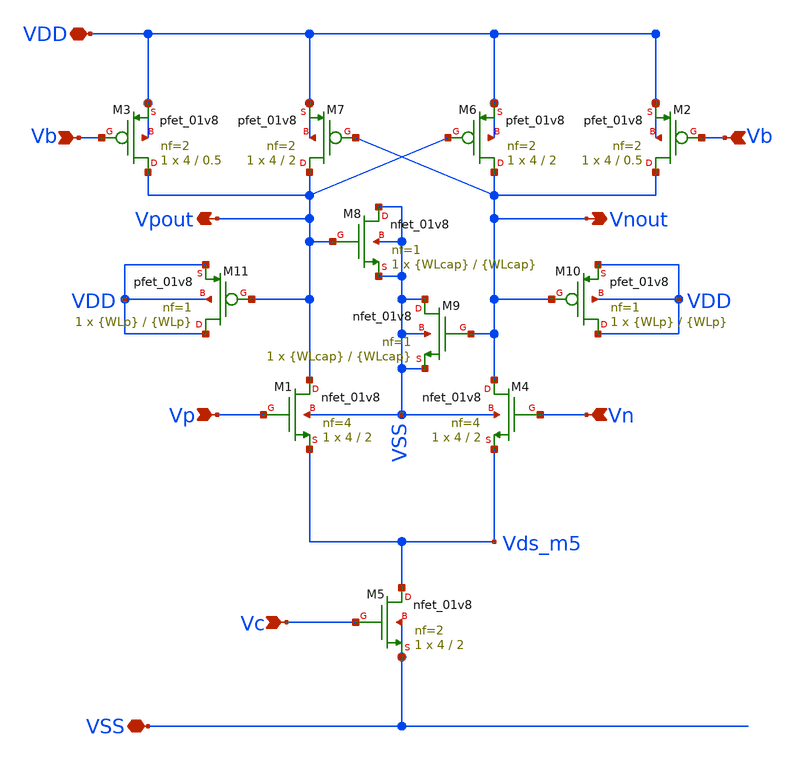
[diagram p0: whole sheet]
** sch_path: xschem/vco_stage_5.sch
**.subckt vco_stage_5 VDD VSS Vp Vn Vb Vc Vpout Vnout Vb
*.iopin VDD
*.iopin VSS
*.ipin Vp
*.ipin Vn
*.ipin Vb
*.ipin Vc
*.opin Vpout
*.opin Vnout
*.ipin Vb
XM1 Vpout Vp Vds_m5 VSS sky130_fd_pr__nfet_01v8 L=2 W=4 nf=4 ad='int((nf+1)/2) * W/nf * 0.29' as='int((nf+2)/2) * W/nf * 0.29'
+ pd='2*int((nf+1)/2) * (W/nf + 0.29)' ps='2*int((nf+2)/2) * (W/nf + 0.29)' nrd='0.29 / W' nrs='0.29 / W'
+ sa=0 sb=0 sd=0 mult=1 m=1
XM4 Vnout Vn Vds_m5 VSS sky130_fd_pr__nfet_01v8 L=2 W=4 nf=4 ad='int((nf+1)/2) * W/nf * 0.29' as='int((nf+2)/2) * W/nf * 0.29'
+ pd='2*int((nf+1)/2) * (W/nf + 0.29)' ps='2*int((nf+2)/2) * (W/nf + 0.29)' nrd='0.29 / W' nrs='0.29 / W'
+ sa=0 sb=0 sd=0 mult=1 m=1
XM5 Vds_m5 Vc VSS VSS sky130_fd_pr__nfet_01v8 L=2 W=4 nf=2 ad='int((nf+1)/2) * W/nf * 0.29' as='int((nf+2)/2) * W/nf * 0.29'
+ pd='2*int((nf+1)/2) * (W/nf + 0.29)' ps='2*int((nf+2)/2) * (W/nf + 0.29)' nrd='0.29 / W' nrs='0.29 / W'
+ sa=0 sb=0 sd=0 mult=1 m=1
XM2 Vnout Vb VDD VDD sky130_fd_pr__pfet_01v8 L=0.5 W=4 nf=2 ad='int((nf+1)/2) * W/nf * 0.29' as='int((nf+2)/2) * W/nf * 0.29'
+ pd='2*int((nf+1)/2) * (W/nf + 0.29)' ps='2*int((nf+2)/2) * (W/nf + 0.29)' nrd='0.29 / W' nrs='0.29 / W'
+ sa=0 sb=0 sd=0 mult=1 m=1
XM3 Vpout Vb VDD VDD sky130_fd_pr__pfet_01v8 L=0.5 W=4 nf=2 ad='int((nf+1)/2) * W/nf * 0.29' as='int((nf+2)/2) * W/nf * 0.29'
+ pd='2*int((nf+1)/2) * (W/nf + 0.29)' ps='2*int((nf+2)/2) * (W/nf + 0.29)' nrd='0.29 / W' nrs='0.29 / W'
+ sa=0 sb=0 sd=0 mult=1 m=1
XM6 Vnout Vpout VDD VDD sky130_fd_pr__pfet_01v8 L=2 W=4 nf=2 ad='int((nf+1)/2) * W/nf * 0.29' as='int((nf+2)/2) * W/nf * 0.29'
+ pd='2*int((nf+1)/2) * (W/nf + 0.29)' ps='2*int((nf+2)/2) * (W/nf + 0.29)' nrd='0.29 / W' nrs='0.29 / W'
+ sa=0 sb=0 sd=0 mult=1 m=1
XM7 Vpout Vnout VDD VDD sky130_fd_pr__pfet_01v8 L=2 W=4 nf=2 ad='int((nf+1)/2) * W/nf * 0.29' as='int((nf+2)/2) * W/nf * 0.29'
+ pd='2*int((nf+1)/2) * (W/nf + 0.29)' ps='2*int((nf+2)/2) * (W/nf + 0.29)' nrd='0.29 / W' nrs='0.29 / W'
+ sa=0 sb=0 sd=0 mult=1 m=1
XM8 VSS Vpout VSS VSS sky130_fd_pr__nfet_01v8 L={WLcap} W={WLcap} nf=1 ad='int((nf+1)/2) * W/nf * 0.29'
+ as='int((nf+2)/2) * W/nf * 0.29' pd='2*int((nf+1)/2) * (W/nf + 0.29)' ps='2*int((nf+2)/2) * (W/nf + 0.29)'
+ nrd='0.29 / W' nrs='0.29 / W' sa=0 sb=0 sd=0 mult=1 m=1
XM9 VSS Vnout VSS VSS sky130_fd_pr__nfet_01v8 L={WLcap} W={WLcap} nf=1 ad='int((nf+1)/2) * W/nf * 0.29'
+ as='int((nf+2)/2) * W/nf * 0.29' pd='2*int((nf+1)/2) * (W/nf + 0.29)' ps='2*int((nf+2)/2) * (W/nf + 0.29)'
+ nrd='0.29 / W' nrs='0.29 / W' sa=0 sb=0 sd=0 mult=1 m=1
XM10 VDD Vnout VDD VDD sky130_fd_pr__pfet_01v8 L={WLp} W={WLp} nf=1 ad='int((nf+1)/2) * W/nf * 0.29'
+ as='int((nf+2)/2) * W/nf * 0.29' pd='2*int((nf+1)/2) * (W/nf + 0.29)' ps='2*int((nf+2)/2) * (W/nf + 0.29)'
+ nrd='0.29 / W' nrs='0.29 / W' sa=0 sb=0 sd=0 mult=1 m=1
XM11 VDD Vpout VDD VDD sky130_fd_pr__pfet_01v8 L={WLp} W={WLp} nf=1 ad='int((nf+1)/2) * W/nf * 0.29'
+ as='int((nf+2)/2) * W/nf * 0.29' pd='2*int((nf+1)/2) * (W/nf + 0.29)' ps='2*int((nf+2)/2) * (W/nf + 0.29)'
+ nrd='0.29 / W' nrs='0.29 / W' sa=0 sb=0 sd=0 mult=1 m=1
**.ends
.end
